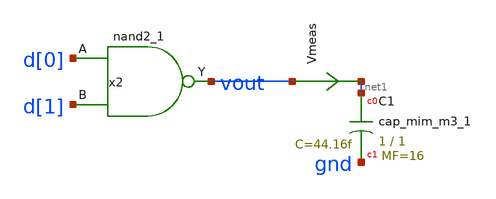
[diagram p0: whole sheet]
** sch_path: xschem/nand-tb.sch
.lib $::SKYWATER_MODELS/sky130.lib.spice tt
.include $::SKYWATER_STDCELLS/sky130_fd_sc_hd.spice

**.subckt nand-tb
XC1 net1 gnd sky130_fd_pr__cap_mim_m3_1 W=1 L=1 MF=16 m=16
Vmeas vout net1 0
.save i(vmeas)
x2 d[0] d[1] GND gnd vdd vdd vout sky130_fd_sc_hd__nand2_1
**** begin user architecture code



  .option wnflag=1
  .option safecurrents
  ********************Static Voltage Sources***************************
  Vddh vdd gnd dc 1.8

  ********************Dynamic Voltage Sources***************************
  *******Calculation**********
  .param base_f=100e3 base_t={1/base_f} base_th={base_t/2} base_d={base_th}
  .param d2_th ={base_th} d2_t={2*d2_th}
  .param d1_th ={4*d2_th} d1_t={d0_th}
  .param d0_th ={4*d1_th} d0_t={4*d0_th}

  .param d20_d ={0} d21_d={1*d2_th} d22_d={2*d2_th} d23_d={3*d2_th}
  .param d10_d ={0} d11_d={1*d1_th} d12_d={2*d1_th} d13_d={3*d1_th}
  .param d00_d ={0} d01_d={1*d0_th} d02_d={2*d0_th} d03_d={3*d0_th}
  *******Signals**********
  .param vhi=1.8
  Vd00 d[0] gnd pulse(0 {vhi} {0} 1p 1p {10u} {20u})
  Vd01 d[1] gnd pulse(0 {vhi} {0} 1p 1p {20u} {40u})
  ********************Simulation Commands*****************************
  .control
     reset
     save all
     tran 1n 50u
     write nand-tb.raw
     set appendwrite
*    quit 0
  .endc



**** end user architecture code
**.ends
.end
